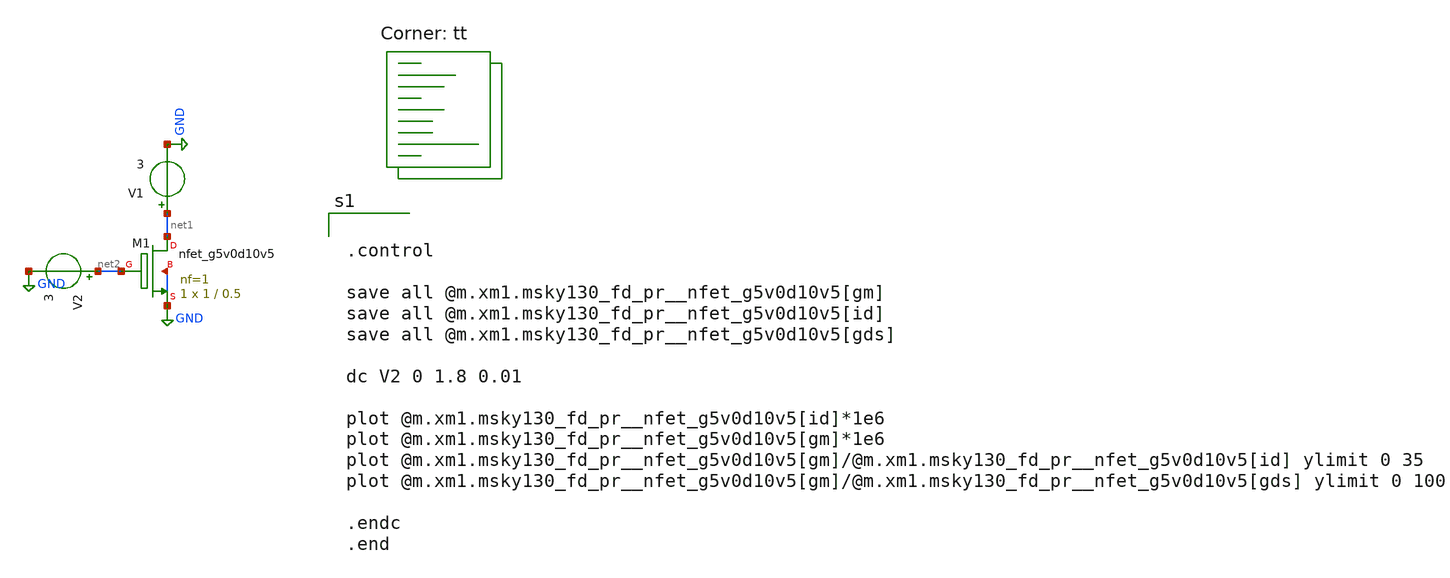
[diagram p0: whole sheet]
** sch_path: analog/schematics/TransAmp.sch
**.subckt TransAmp
V1 net1 GND 3
V2 net2 GND 3
XM1 net1 net2 GND GND sky130_fd_pr__nfet_g5v0d10v5 L=0.5 W=1 nf=1 ad='int((nf+1)/2) * W/nf * 0.29' as='int((nf+2)/2) * W/nf * 0.29'
+ pd='2*int((nf+1)/2) * (W/nf + 0.29)' ps='2*int((nf+2)/2) * (W/nf + 0.29)' nrd='0.29 / W' nrs='0.29 / W'
+ sa=0 sb=0 sd=0 mult=1 m=1
**** begin user architecture code


.control

save all @m.xm1.msky130_fd_pr__nfet_g5v0d10v5[gm]
save all @m.xm1.msky130_fd_pr__nfet_g5v0d10v5[id]
save all @m.xm1.msky130_fd_pr__nfet_g5v0d10v5[gds]

dc V2 0 1.8 0.01

plot @m.xm1.msky130_fd_pr__nfet_g5v0d10v5[id]*1e6
plot @m.xm1.msky130_fd_pr__nfet_g5v0d10v5[gm]*1e6
plot @m.xm1.msky130_fd_pr__nfet_g5v0d10v5[gm]/@m.xm1.msky130_fd_pr__nfet_g5v0d10v5[id] ylimit 0 35
plot @m.xm1.msky130_fd_pr__nfet_g5v0d10v5[gm]/@m.xm1.msky130_fd_pr__nfet_g5v0d10v5[gds] ylimit 0 100

.endc
.end


.lib $::SKYWATER_MODELS/sky130.lib.spice tt
**** end user architecture code
**.ends
.GLOBAL GND
.end
